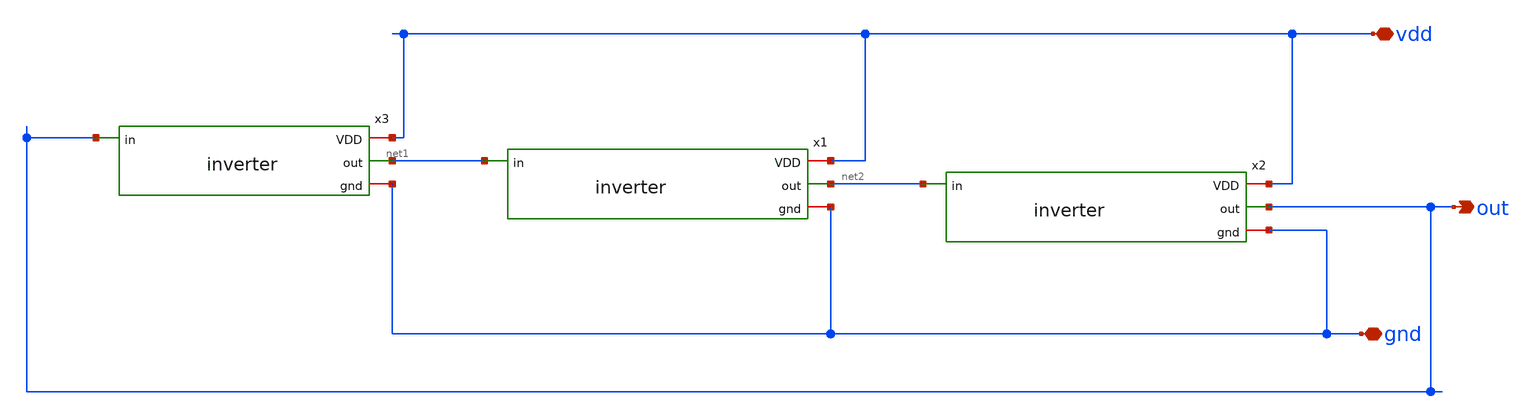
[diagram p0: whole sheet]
** sch_path: ringosc/ringosc.sch
**.subckt ringosc out gnd vdd
*.opin out
*.iopin gnd
*.iopin vdd
x1 vdd net1 net2 gnd inverter
x2 vdd net2 out gnd inverter
x3 vdd out net1 gnd inverter
**.ends

* expanding   symbol:  /home/chandra_hartono/project/inverter/inverter.sym # of pins=4
** sym_path: inverter/inverter.sym
** sch_path: inverter/inverter.sch
.subckt inverter VDD in out gnd
*.ipin in
*.opin out
*.iopin VDD
*.iopin gnd
XM1 out in gnd gnd sky130_fd_pr__nfet_01v8 L=0.15 W=1 nf=1 ad='int((nf+1)/2) * W/nf * 0.29' as='int((nf+2)/2) * W/nf * 0.29'
+ pd='2*int((nf+1)/2) * (W/nf + 0.29)' ps='2*int((nf+2)/2) * (W/nf + 0.29)' nrd='0.29 / W' nrs='0.29 / W'
+ sa=0 sb=0 sd=0 mult=1 m=1
XM2 out in VDD VDD sky130_fd_pr__pfet_01v8 L=0.15 W=1 nf=1 ad='int((nf+1)/2) * W/nf * 0.29' as='int((nf+2)/2) * W/nf * 0.29'
+ pd='2*int((nf+1)/2) * (W/nf + 0.29)' ps='2*int((nf+2)/2) * (W/nf + 0.29)' nrd='0.29 / W' nrs='0.29 / W'
+ sa=0 sb=0 sd=0 mult=1 m=1
.ends

.end
